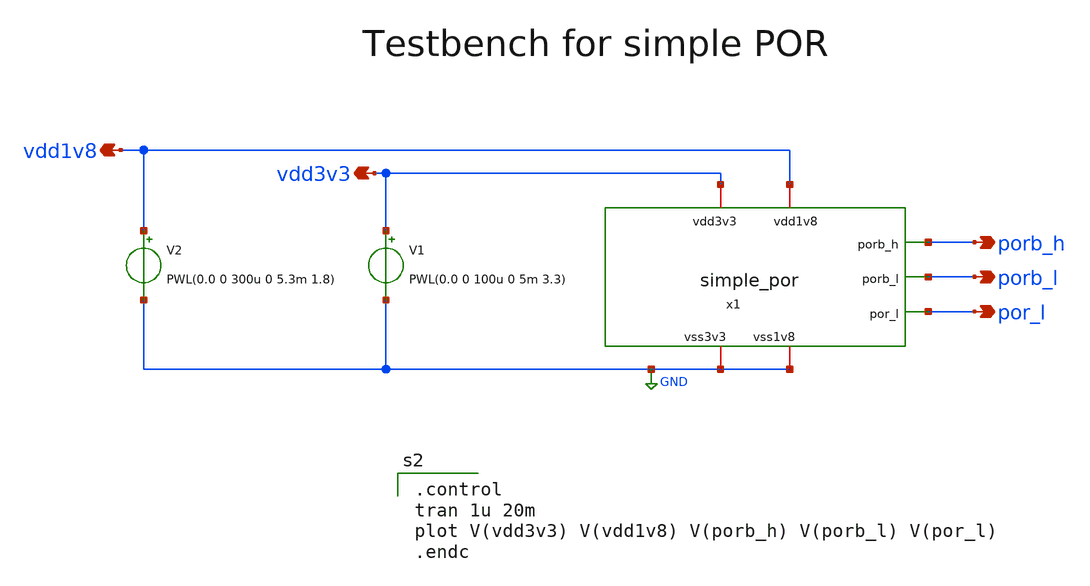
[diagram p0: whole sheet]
** sch_path: xschem/simple_por_tb.sch
**.subckt simple_por_tb vdd3v3 vdd1v8 porb_h porb_l por_l
*.opin vdd3v3
*.opin vdd1v8
*.opin porb_h
*.opin porb_l
*.opin por_l
x1 vdd3v3 vdd1v8 porb_h porb_l por_l GND GND simple_por
V1 vdd3v3 GND PWL(0.0 0 100u 0 5m 3.3)
V2 vdd1v8 GND PWL(0.0 0 300u 0 5.3m 1.8)
**** begin user architecture code
.lib $::SKYWATER_MODELS/sky130.lib.spice tt
.include $::PDKPATH/libs.ref/sky130_fd_sc_hvl/spice/sky130_fd_sc_hvl.spice

.control
tran 1u 20m
plot V(vdd3v3) V(vdd1v8) V(porb_h) V(porb_l) V(por_l)
.endc

**** end user architecture code
**.ends

* expanding   symbol:  simple_por.sym # of pins=7
** sym_path: xschem/simple_por.sym
** sch_path: xschem/simple_por.sch
.subckt simple_por vdd3v3 vdd1v8 porb_h porb_l por_l vss3v3 vss1v8
*.iopin vdd3v3
*.iopin vss3v3
*.opin porb_h
*.opin porb_l
*.opin por_l
*.iopin vdd1v8
*.iopin vss1v8
XC1 net9 vss3v3 sky130_fd_pr__cap_mim_m3_1 W=30 L=30 MF=1 m=1
XC2 vss3v3 net9 sky130_fd_pr__cap_mim_m3_2 W=30 L=30 MF=1 m=1
XM1 net3 net7 net5 vdd3v3 sky130_fd_pr__pfet_g5v0d10v5 L=0.8 W=2 nf=1 ad='int((nf+1)/2) * W/nf * 0.29'
+ as='int((nf+2)/2) * W/nf * 0.29' pd='2*int((nf+1)/2) * (W/nf + 0.29)' ps='2*int((nf+2)/2) * (W/nf + 0.29)'
+ nrd='0.29 / W' nrs='0.29 / W' sa=0 sb=0 sd=0 mult=1 m=1
XM2 net2 net3 vss3v3 vss3v3 sky130_fd_pr__nfet_g5v0d10v5 L=0.8 W=2 nf=1 ad='int((nf+1)/2) * W/nf * 0.29'
+ as='int((nf+2)/2) * W/nf * 0.29' pd='2*int((nf+1)/2) * (W/nf + 0.29)' ps='2*int((nf+2)/2) * (W/nf + 0.29)'
+ nrd='0.29 / W' nrs='0.29 / W' sa=0 sb=0 sd=0 mult=1 m=1
XR1 net4 vdd3v3 vss3v3 sky130_fd_pr__res_xhigh_po_0p69 L=500 mult=1 m=1
XM4 net5 net6 vdd3v3 vdd3v3 sky130_fd_pr__pfet_g5v0d10v5 L=0.8 W=2 nf=1 ad='int((nf+1)/2) * W/nf * 0.29'
+ as='int((nf+2)/2) * W/nf * 0.29' pd='2*int((nf+1)/2) * (W/nf + 0.29)' ps='2*int((nf+2)/2) * (W/nf + 0.29)'
+ nrd='0.29 / W' nrs='0.29 / W' sa=0 sb=0 sd=0 mult=1 m=1
XM5 net3 net3 vss3v3 vss3v3 sky130_fd_pr__nfet_g5v0d10v5 L=0.8 W=14 nf=7 ad='int((nf+1)/2) * W/nf * 0.29'
+ as='int((nf+2)/2) * W/nf * 0.29' pd='2*int((nf+1)/2) * (W/nf + 0.29)' ps='2*int((nf+2)/2) * (W/nf + 0.29)'
+ nrd='0.29 / W' nrs='0.29 / W' sa=0 sb=0 sd=0 mult=1 m=1
XR2 vss3v3 net4 vss3v3 sky130_fd_pr__res_xhigh_po_0p69 L=150 mult=1 m=1
XM7 net2 net2 net1 vdd3v3 sky130_fd_pr__pfet_g5v0d10v5 L=0.8 W=2 nf=1 ad='int((nf+1)/2) * W/nf * 0.29'
+ as='int((nf+2)/2) * W/nf * 0.29' pd='2*int((nf+1)/2) * (W/nf + 0.29)' ps='2*int((nf+2)/2) * (W/nf + 0.29)'
+ nrd='0.29 / W' nrs='0.29 / W' sa=0 sb=0 sd=0 mult=1 m=1
XM8 net1 net1 vdd3v3 vdd3v3 sky130_fd_pr__pfet_g5v0d10v5 L=0.8 W=14 nf=7 ad='int((nf+1)/2) * W/nf * 0.29'
+ as='int((nf+2)/2) * W/nf * 0.29' pd='2*int((nf+1)/2) * (W/nf + 0.29)' ps='2*int((nf+2)/2) * (W/nf + 0.29)'
+ nrd='0.29 / W' nrs='0.29 / W' sa=0 sb=0 sd=0 mult=1 m=1
XM10 net7 net4 vss3v3 vss3v3 sky130_fd_pr__nfet_g5v0d10v5 L=0.8 W=2 nf=1 ad='int((nf+1)/2) * W/nf * 0.29'
+ as='int((nf+2)/2) * W/nf * 0.29' pd='2*int((nf+1)/2) * (W/nf + 0.29)' ps='2*int((nf+2)/2) * (W/nf + 0.29)'
+ nrd='0.29 / W' nrs='0.29 / W' sa=0 sb=0 sd=0 mult=1 m=1
XM9 net7 net7 net6 vdd3v3 sky130_fd_pr__pfet_g5v0d10v5 L=0.8 W=2 nf=1 ad='int((nf+1)/2) * W/nf * 0.29'
+ as='int((nf+2)/2) * W/nf * 0.29' pd='2*int((nf+1)/2) * (W/nf + 0.29)' ps='2*int((nf+2)/2) * (W/nf + 0.29)'
+ nrd='0.29 / W' nrs='0.29 / W' sa=0 sb=0 sd=0 mult=1 m=1
XM11 net6 net6 vdd3v3 vdd3v3 sky130_fd_pr__pfet_g5v0d10v5 L=0.8 W=16 nf=8 ad='int((nf+1)/2) * W/nf * 0.29'
+ as='int((nf+2)/2) * W/nf * 0.29' pd='2*int((nf+1)/2) * (W/nf + 0.29)' ps='2*int((nf+2)/2) * (W/nf + 0.29)'
+ nrd='0.29 / W' nrs='0.29 / W' sa=0 sb=0 sd=0 mult=1 m=1
XM12 net8 net1 vdd3v3 vdd3v3 sky130_fd_pr__pfet_g5v0d10v5 L=0.8 W=2 nf=1 ad='int((nf+1)/2) * W/nf * 0.29'
+ as='int((nf+2)/2) * W/nf * 0.29' pd='2*int((nf+1)/2) * (W/nf + 0.29)' ps='2*int((nf+2)/2) * (W/nf + 0.29)'
+ nrd='0.29 / W' nrs='0.29 / W' sa=0 sb=0 sd=0 mult=1 m=1
XM13 net9 net2 net8 vdd3v3 sky130_fd_pr__pfet_g5v0d10v5 L=0.8 W=2 nf=1 ad='int((nf+1)/2) * W/nf * 0.29'
+ as='int((nf+2)/2) * W/nf * 0.29' pd='2*int((nf+1)/2) * (W/nf + 0.29)' ps='2*int((nf+2)/2) * (W/nf + 0.29)'
+ nrd='0.29 / W' nrs='0.29 / W' sa=0 sb=0 sd=0 mult=1 m=1
XR3 vss3v3 vss3v3 vss3v3 sky130_fd_pr__res_xhigh_po_0p69 L=25 mult=2 m=2
x2 net10 vss3v3 vss3v3 vdd3v3 vdd3v3 porb_h sky130_fd_sc_hvl__buf_8
x3 net10 vss1v8 vss1v8 vdd1v8 vdd1v8 porb_l sky130_fd_sc_hvl__buf_8
x4 net10 vss1v8 vss1v8 vdd1v8 vdd1v8 por_l sky130_fd_sc_hvl__inv_8
x5 net9 vss3v3 vss3v3 vdd3v3 vdd3v3 net10 sky130_fd_sc_hvl__schmittbuf_1
.ends

.GLOBAL GND
.end
